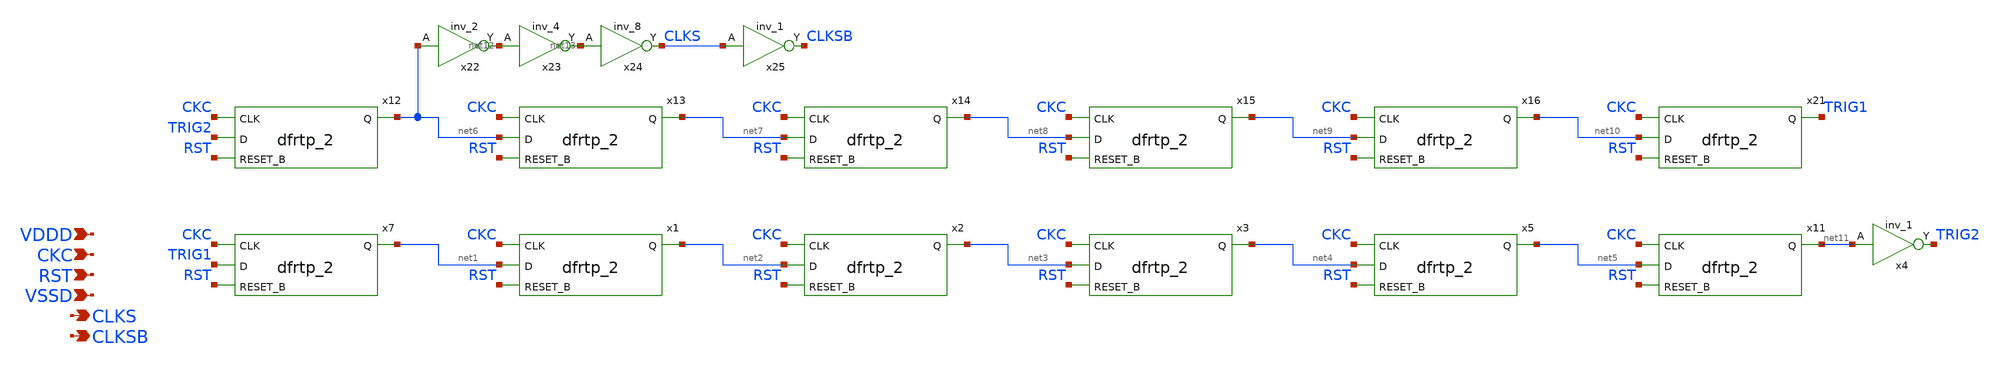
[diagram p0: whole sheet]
** sch_path: xschem/auto_sampling.sch
**.subckt auto_sampling CKC VDDD VSSD CLKS CLKSB RST
*.ipin CKC
*.ipin VDDD
*.ipin VSSD
*.opin CLKS
*.opin CLKSB
*.ipin RST
x7 CKC TRIG1 RST VSSD VSSD VDDD VDDD net1 sky130_fd_sc_hdll__dfrtp_2
x1 CKC net1 RST VSSD VSSD VDDD VDDD net2 sky130_fd_sc_hdll__dfrtp_2
x2 CKC net2 RST VSSD VSSD VDDD VDDD net3 sky130_fd_sc_hdll__dfrtp_2
x3 CKC net3 RST VSSD VSSD VDDD VDDD net4 sky130_fd_sc_hdll__dfrtp_2
x5 CKC net4 RST VSSD VSSD VDDD VDDD net5 sky130_fd_sc_hdll__dfrtp_2
x11 CKC net5 RST VSSD VSSD VDDD VDDD net11 sky130_fd_sc_hdll__dfrtp_2
x12 CKC TRIG2 RST VSSD VSSD VDDD VDDD net6 sky130_fd_sc_hdll__dfrtp_2
x13 CKC net6 RST VSSD VSSD VDDD VDDD net7 sky130_fd_sc_hdll__dfrtp_2
x14 CKC net7 RST VSSD VSSD VDDD VDDD net8 sky130_fd_sc_hdll__dfrtp_2
x15 CKC net8 RST VSSD VSSD VDDD VDDD net9 sky130_fd_sc_hdll__dfrtp_2
x16 CKC net9 RST VSSD VSSD VDDD VDDD net10 sky130_fd_sc_hdll__dfrtp_2
x21 CKC net10 RST VSSD VSSD VDDD VDDD TRIG1 sky130_fd_sc_hdll__dfrtp_2
x22 net6 VSSD VSSD VDDD VDDD net12 sky130_fd_sc_hdll__inv_2
x23 net12 VSSD VSSD VDDD VDDD net13 sky130_fd_sc_hdll__inv_4
x24 net13 VSSD VSSD VDDD VDDD CLKS sky130_fd_sc_hdll__inv_8
x25 CLKS VSSD VSSD VDDD VDDD CLKSB sky130_fd_sc_hdll__inv_1
x4 net11 VSSD VSSD VDDD VDDD TRIG2 sky130_fd_sc_hdll__inv_1
**.ends
.end
